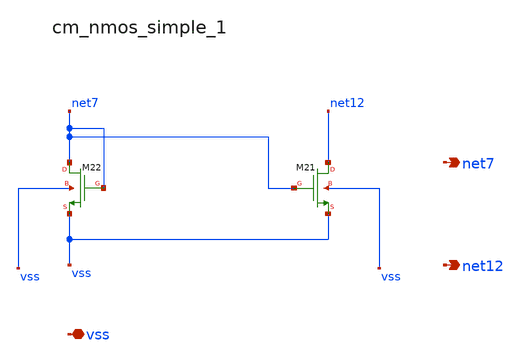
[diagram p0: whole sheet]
** sch_path: analog-db/raw/ldo_001_analoggym_basic/hier/blocks/cm_nmos_simple_1.sch
**.subckt cm_nmos_simple_1 vss net7 net12
*.iopin vss
*.opin net7
*.opin net12
XM21 net12 net7 vss vss sg13_lv_nmos w=x_dut_xm21_w l=x_dut_xm21_l ng=1 m=x_dut_xm21_m
XM22 net7 net7 vss vss sg13_lv_nmos w=x_dut_xm22_w l=x_dut_xm22_l ng=1 m=x_dut_xm22_m
**.ends
.end
